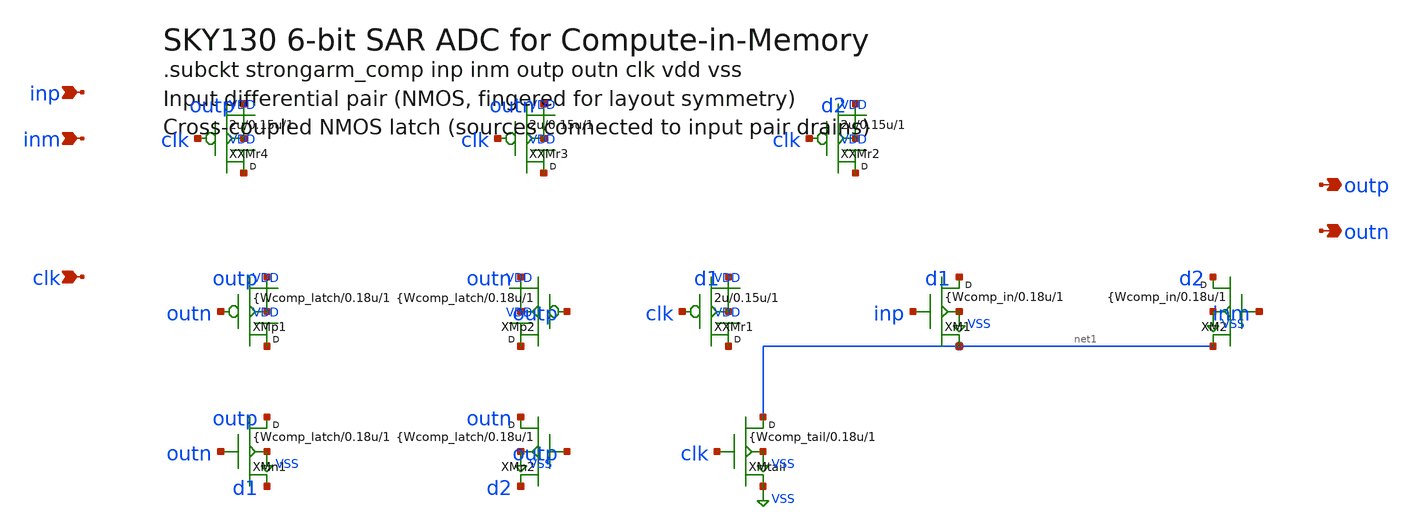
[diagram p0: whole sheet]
** sch_path: data/sch/cim_adc.sch
**.subckt cim_adc inp inm outp outn clk
*.ipin inp
*.ipin inm
*.opin outp
*.opin outn
*.ipin clk
XMtail net1 clk VSS VSS nmos w={Wcomp_tail l=0.18u m=1
XM1 d1 inp net1 VSS nmos w={Wcomp_in l=0.18u m=1
XM2 d2 inm net1 VSS nmos w={Wcomp_in l=0.18u m=1
XXMr1 VDD clk d1 VDD sky130_fd_pr__pfet_01v8 w=2u l=0.15u m=1
XXMr2 VDD clk d2 VDD sky130_fd_pr__pfet_01v8 w=2u l=0.15u m=1
XXMr3 VDD clk outn VDD sky130_fd_pr__pfet_01v8 w=2u l=0.15u m=1
XXMr4 VDD clk outp VDD sky130_fd_pr__pfet_01v8 w=2u l=0.15u m=1
XMp1 VDD outn outp VDD pmos w={Wcomp_latch l=0.18u m=1
XMp2 VDD outp outn VDD pmos w={Wcomp_latch l=0.18u m=1
XMn1 outp outn d1 VSS nmos w={Wcomp_latch l=0.18u m=1
XMn2 outn outp d2 VSS nmos w={Wcomp_latch l=0.18u m=1
**.ends
.GLOBAL VSS
.GLOBAL VDD
.end
